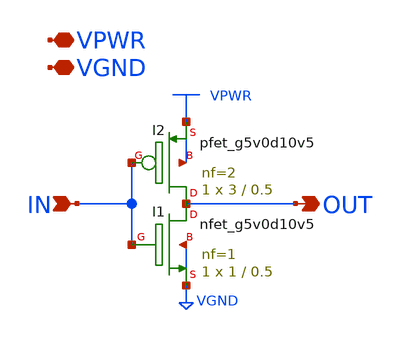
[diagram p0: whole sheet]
** sch_path: gpiov2_amux_ls_inv_x1.sch
* Copyright 2023 David Mitchell Bailey
* Licensed under the Apache License, Version 2.0 (the "License");
* you may not use this file except in compliance with the License.
* You may obtain a copy of the License at
* https://www.apache.org/licenses/LICENSE-2.0
* Unless required by applicable law or agreed to in writing, software
* distributed under the License is distributed on an "AS IS" BASIS,
* WITHOUT WARRANTIES OR CONDITIONS OF ANY KIND, either express or implied.
* See the License for the specific language governing permissions and
* limitations under the License.
**.subckt gpiov2_amux_ls_inv_x1 IN OUT VPWR VGND
*.ipin IN
*.opin OUT
*.iopin VPWR
*.iopin VGND
XI1 OUT IN VGND VGND sky130_fd_pr__nfet_g5v0d10v5 L=0.5 W=1 nf=1 ad='int((nf+1)/2) * W/nf * 0.29' as='int((nf+2)/2) * W/nf * 0.29'
+ pd='2*int((nf+1)/2) * (W/nf + 0.29)' ps='2*int((nf+2)/2) * (W/nf + 0.29)' nrd='0.29 / W' nrs='0.29 / W'
+ sa=0 sb=0 sd=0 mult=1 m=1
XI2 OUT IN VPWR VPWR sky130_fd_pr__pfet_g5v0d10v5 L=0.5 W=3 nf=2 ad='int((nf+1)/2) * W/nf * 0.29' as='int((nf+2)/2) * W/nf * 0.29'
+ pd='2*int((nf+1)/2) * (W/nf + 0.29)' ps='2*int((nf+2)/2) * (W/nf + 0.29)' nrd='0.29 / W' nrs='0.29 / W'
+ sa=0 sb=0 sd=0 mult=1 m=1
**.ends
.end
